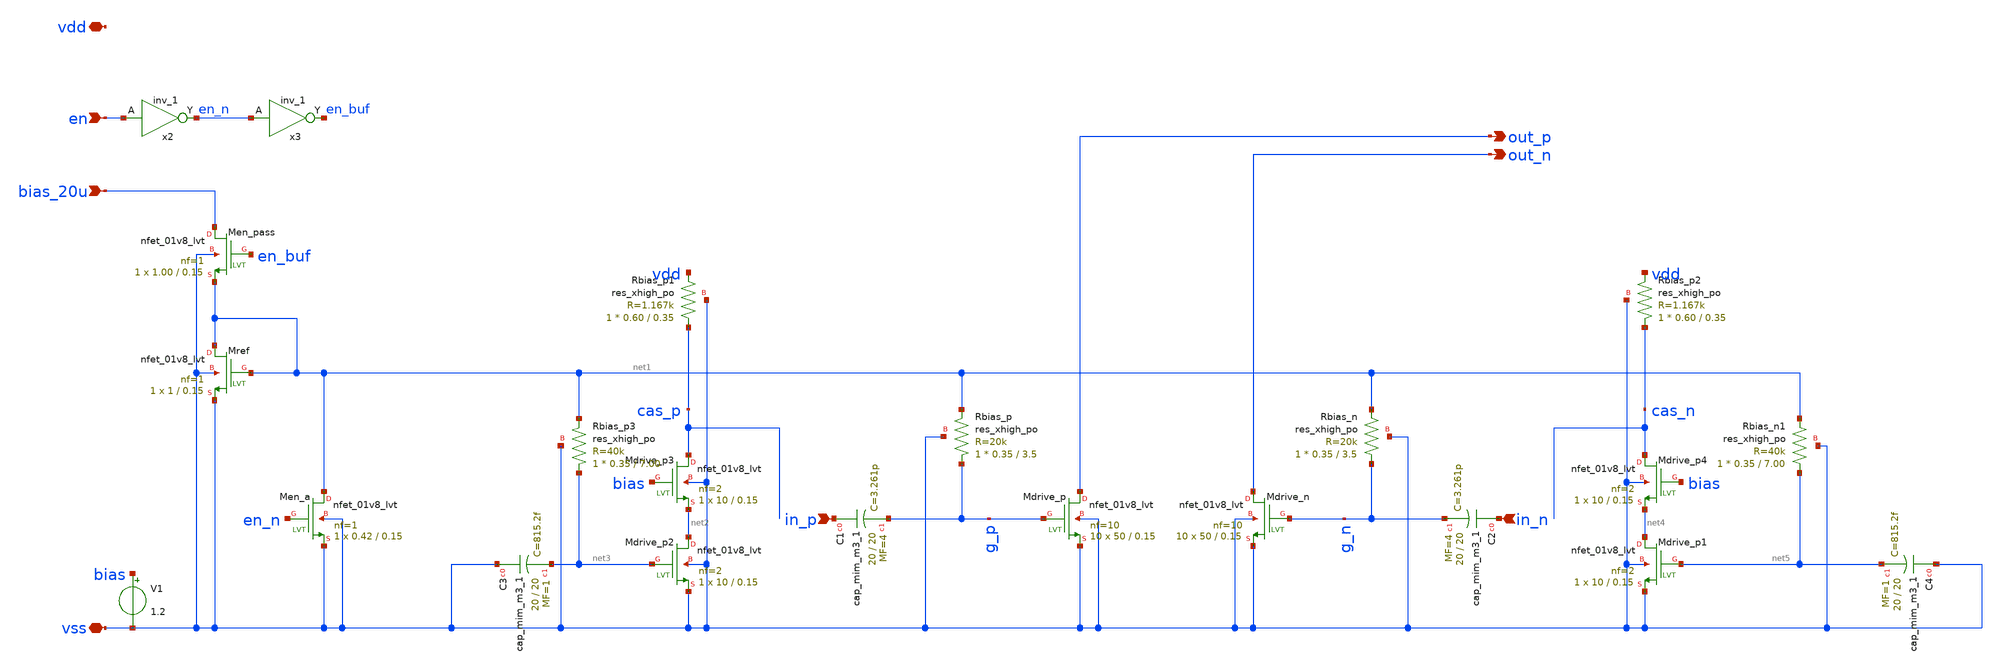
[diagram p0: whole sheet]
** sch_path: design/io_driver/io_driver.sch
**.subckt io_driver en bias_20u vss vdd out_p out_n in_n in_p
*.ipin en
*.ipin bias_20u
*.iopin vss
*.iopin vdd
*.opin out_p
*.opin out_n
*.ipin in_n
*.ipin in_p
XMdrive_p out_p g_p vss vss sky130_fd_pr__nfet_01v8_lvt L=0.15 W=50 nf=10 ad='int((nf+1)/2) * W/nf * 0.29'
+ as='int((nf+2)/2) * W/nf * 0.29' pd='2*int((nf+1)/2) * (W/nf + 0.29)' ps='2*int((nf+2)/2) * (W/nf + 0.29)'
+ nrd='0.29 / W' nrs='0.29 / W' sa=0 sb=0 sd=0 mult=10 m=10
XMdrive_n out_n g_n vss vss sky130_fd_pr__nfet_01v8_lvt L=0.15 W=50 nf=10 ad='int((nf+1)/2) * W/nf * 0.29'
+ as='int((nf+2)/2) * W/nf * 0.29' pd='2*int((nf+1)/2) * (W/nf + 0.29)' ps='2*int((nf+2)/2) * (W/nf + 0.29)'
+ nrd='0.29 / W' nrs='0.29 / W' sa=0 sb=0 sd=0 mult=10 m=10
XMref net1 net1 vss vss sky130_fd_pr__nfet_01v8_lvt L=0.15 W=1 nf=1 ad='int((nf+1)/2) * W/nf * 0.29'
+ as='int((nf+2)/2) * W/nf * 0.29' pd='2*int((nf+1)/2) * (W/nf + 0.29)' ps='2*int((nf+2)/2) * (W/nf + 0.29)'
+ nrd='0.29 / W' nrs='0.29 / W' sa=0 sb=0 sd=0 mult=1 m=1
XMen_pass bias_20u en_buf net1 vss sky130_fd_pr__nfet_01v8_lvt L=0.15 W=1.00 nf=1 ad='int((nf+1)/2) * W/nf * 0.29'
+ as='int((nf+2)/2) * W/nf * 0.29' pd='2*int((nf+1)/2) * (W/nf + 0.29)' ps='2*int((nf+2)/2) * (W/nf + 0.29)'
+ nrd='0.29 / W' nrs='0.29 / W' sa=0 sb=0 sd=0 mult=1 m=1
XMen_a net1 en_n vss vss sky130_fd_pr__nfet_01v8_lvt L=0.15 W=0.42 nf=1 ad='int((nf+1)/2) * W/nf * 0.29'
+ as='int((nf+2)/2) * W/nf * 0.29' pd='2*int((nf+1)/2) * (W/nf + 0.29)' ps='2*int((nf+2)/2) * (W/nf + 0.29)'
+ nrd='0.29 / W' nrs='0.29 / W' sa=0 sb=0 sd=0 mult=1 m=1
x2 en vss vss vdd vdd en_n sky130_fd_sc_hs__inv_1
x3 en_n vss vss vdd vdd en_buf sky130_fd_sc_hs__inv_1
XC1 in_p g_p sky130_fd_pr__cap_mim_m3_1 W=20 L=20 MF=4 m=4
XC2 in_n g_n sky130_fd_pr__cap_mim_m3_1 W=20 L=20 MF=4 m=4
XRbias_p g_p net1 vss sky130_fd_pr__res_xhigh_po W=0.35 L=3.5 mult=1 m=1
XRbias_n g_n net1 vss sky130_fd_pr__res_xhigh_po W=0.35 L=3.5 mult=1 m=1
XMdrive_p2 net2 net3 vss vss sky130_fd_pr__nfet_01v8_lvt L=0.15 W=10 nf=2 ad='int((nf+1)/2) * W/nf * 0.29'
+ as='int((nf+2)/2) * W/nf * 0.29' pd='2*int((nf+1)/2) * (W/nf + 0.29)' ps='2*int((nf+2)/2) * (W/nf + 0.29)'
+ nrd='0.29 / W' nrs='0.29 / W' sa=0 sb=0 sd=0 mult=1 m=1
XMdrive_p3 cas_p bias net2 vss sky130_fd_pr__nfet_01v8_lvt L=0.15 W=10 nf=2 ad='int((nf+1)/2) * W/nf * 0.29'
+ as='int((nf+2)/2) * W/nf * 0.29' pd='2*int((nf+1)/2) * (W/nf + 0.29)' ps='2*int((nf+2)/2) * (W/nf + 0.29)'
+ nrd='0.29 / W' nrs='0.29 / W' sa=0 sb=0 sd=0 mult=1 m=1
XRbias_p1 cas_p vdd vss sky130_fd_pr__res_xhigh_po W=0.60 L=0.35 mult=1 m=1
XMdrive_p1 net4 net5 vss vss sky130_fd_pr__nfet_01v8_lvt L=0.15 W=10 nf=2 ad='int((nf+1)/2) * W/nf * 0.29'
+ as='int((nf+2)/2) * W/nf * 0.29' pd='2*int((nf+1)/2) * (W/nf + 0.29)' ps='2*int((nf+2)/2) * (W/nf + 0.29)'
+ nrd='0.29 / W' nrs='0.29 / W' sa=0 sb=0 sd=0 mult=1 m=1
XMdrive_p4 cas_n bias net4 vss sky130_fd_pr__nfet_01v8_lvt L=0.15 W=10 nf=2 ad='int((nf+1)/2) * W/nf * 0.29'
+ as='int((nf+2)/2) * W/nf * 0.29' pd='2*int((nf+1)/2) * (W/nf + 0.29)' ps='2*int((nf+2)/2) * (W/nf + 0.29)'
+ nrd='0.29 / W' nrs='0.29 / W' sa=0 sb=0 sd=0 mult=1 m=1
XRbias_p2 cas_n vdd vss sky130_fd_pr__res_xhigh_po W=0.60 L=0.35 mult=1 m=1
XC3 vss net3 sky130_fd_pr__cap_mim_m3_1 W=20 L=20 MF=1 m=1
XC4 vss net5 sky130_fd_pr__cap_mim_m3_1 W=20 L=20 MF=1 m=1
XRbias_p3 net3 net1 vss sky130_fd_pr__res_xhigh_po W=0.35 L=7.00 mult=1 m=1
XRbias_n1 net5 net1 vss sky130_fd_pr__res_xhigh_po W=0.35 L=7.00 mult=1 m=1
V1 bias vss 1.2
**.ends
.end
